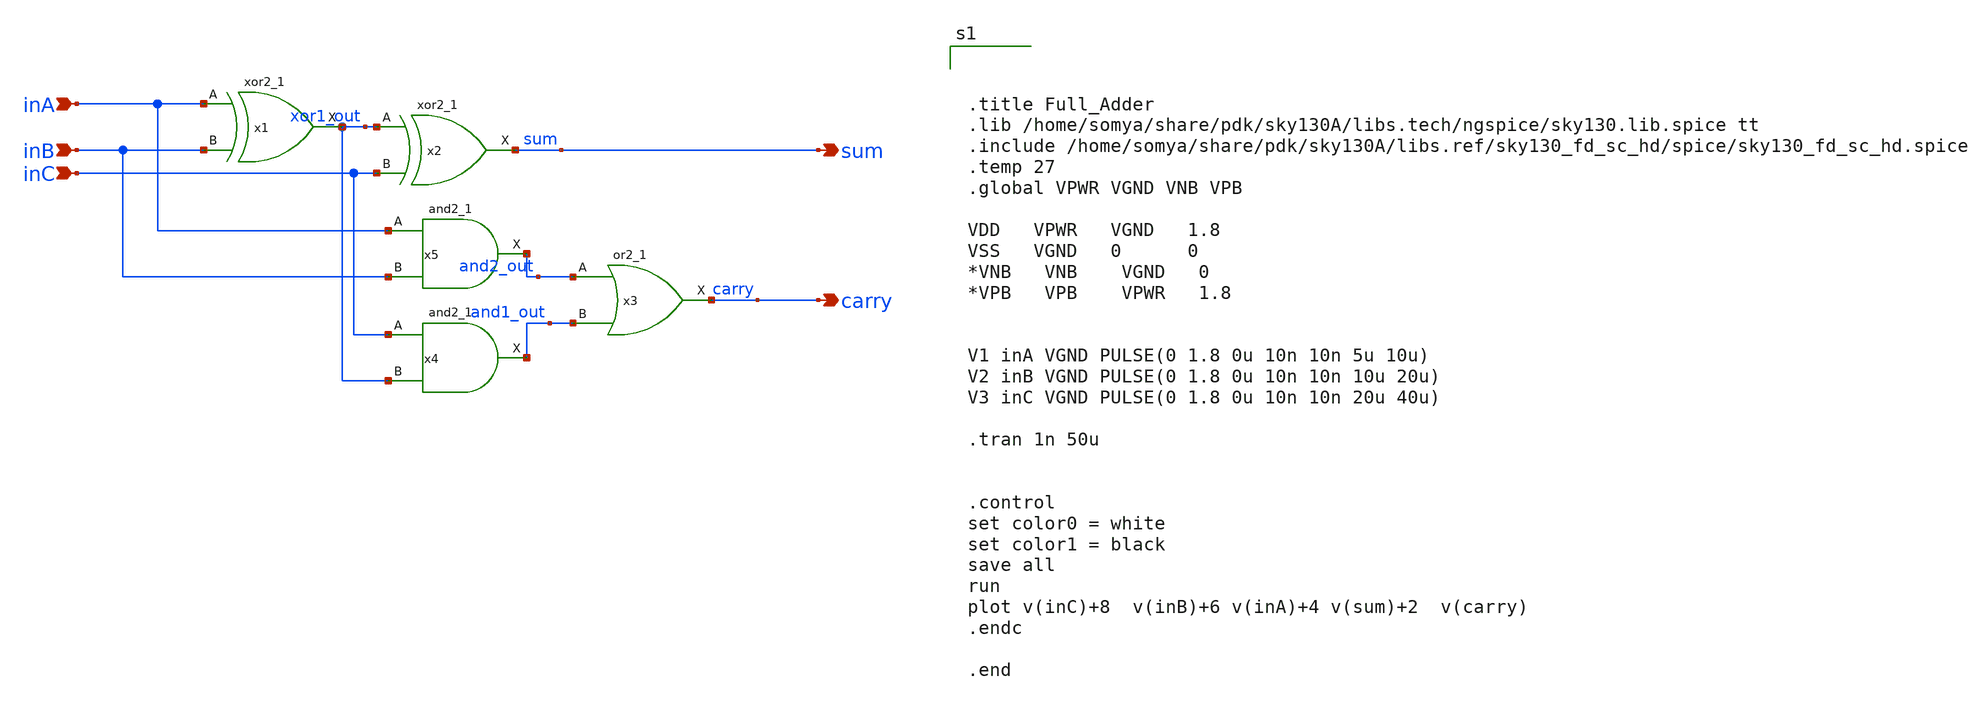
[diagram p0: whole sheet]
** sch_path: NES-2026/STDCELLS/xschem/full_adder_sc.sch
**.subckt full_adder_sc inA inB inC sum carry
*.ipin inA
*.ipin inB
*.ipin inC
*.opin sum
*.opin carry
x1 inA inB VGND VNB VPB VPWR xor1_out sky130_fd_sc_hd__xor2_1
x2 xor1_out inC VGND VNB VPB VPWR sum sky130_fd_sc_hd__xor2_1
x3 and2_out and1_out VGND VNB VPB VPWR carry sky130_fd_sc_hd__or2_1
x5 inA inB VGND VNB VPB VPWR and2_out sky130_fd_sc_hd__and2_1
x4 inC xor1_out VGND VNB VPB VPWR and1_out sky130_fd_sc_hd__and2_1
**** begin user architecture code



.title Full_Adder
.lib /home/somya/share/pdk/sky130A/libs.tech/ngspice/sky130.lib.spice tt
.include /home/somya/share/pdk/sky130A/libs.ref/sky130_fd_sc_hd/spice/sky130_fd_sc_hd.spice
.temp 27
.global VPWR VGND VNB VPB

VDD   VPWR   VGND   1.8
VSS   VGND   0      0
*VNB   VNB    VGND   0
*VPB   VPB    VPWR   1.8


V1 inA VGND PULSE(0 1.8 0u 10n 10n 5u 10u)
V2 inB VGND PULSE(0 1.8 0u 10n 10n 10u 20u)
V3 inC VGND PULSE(0 1.8 0u 10n 10n 20u 40u)

.tran 1n 50u


.control
set color0 = white
set color1 = black
save all
run
plot v(inC)+8  v(inB)+6 v(inA)+4 v(sum)+2  v(carry)
.endc

.end


**** end user architecture code
**.ends
.end
